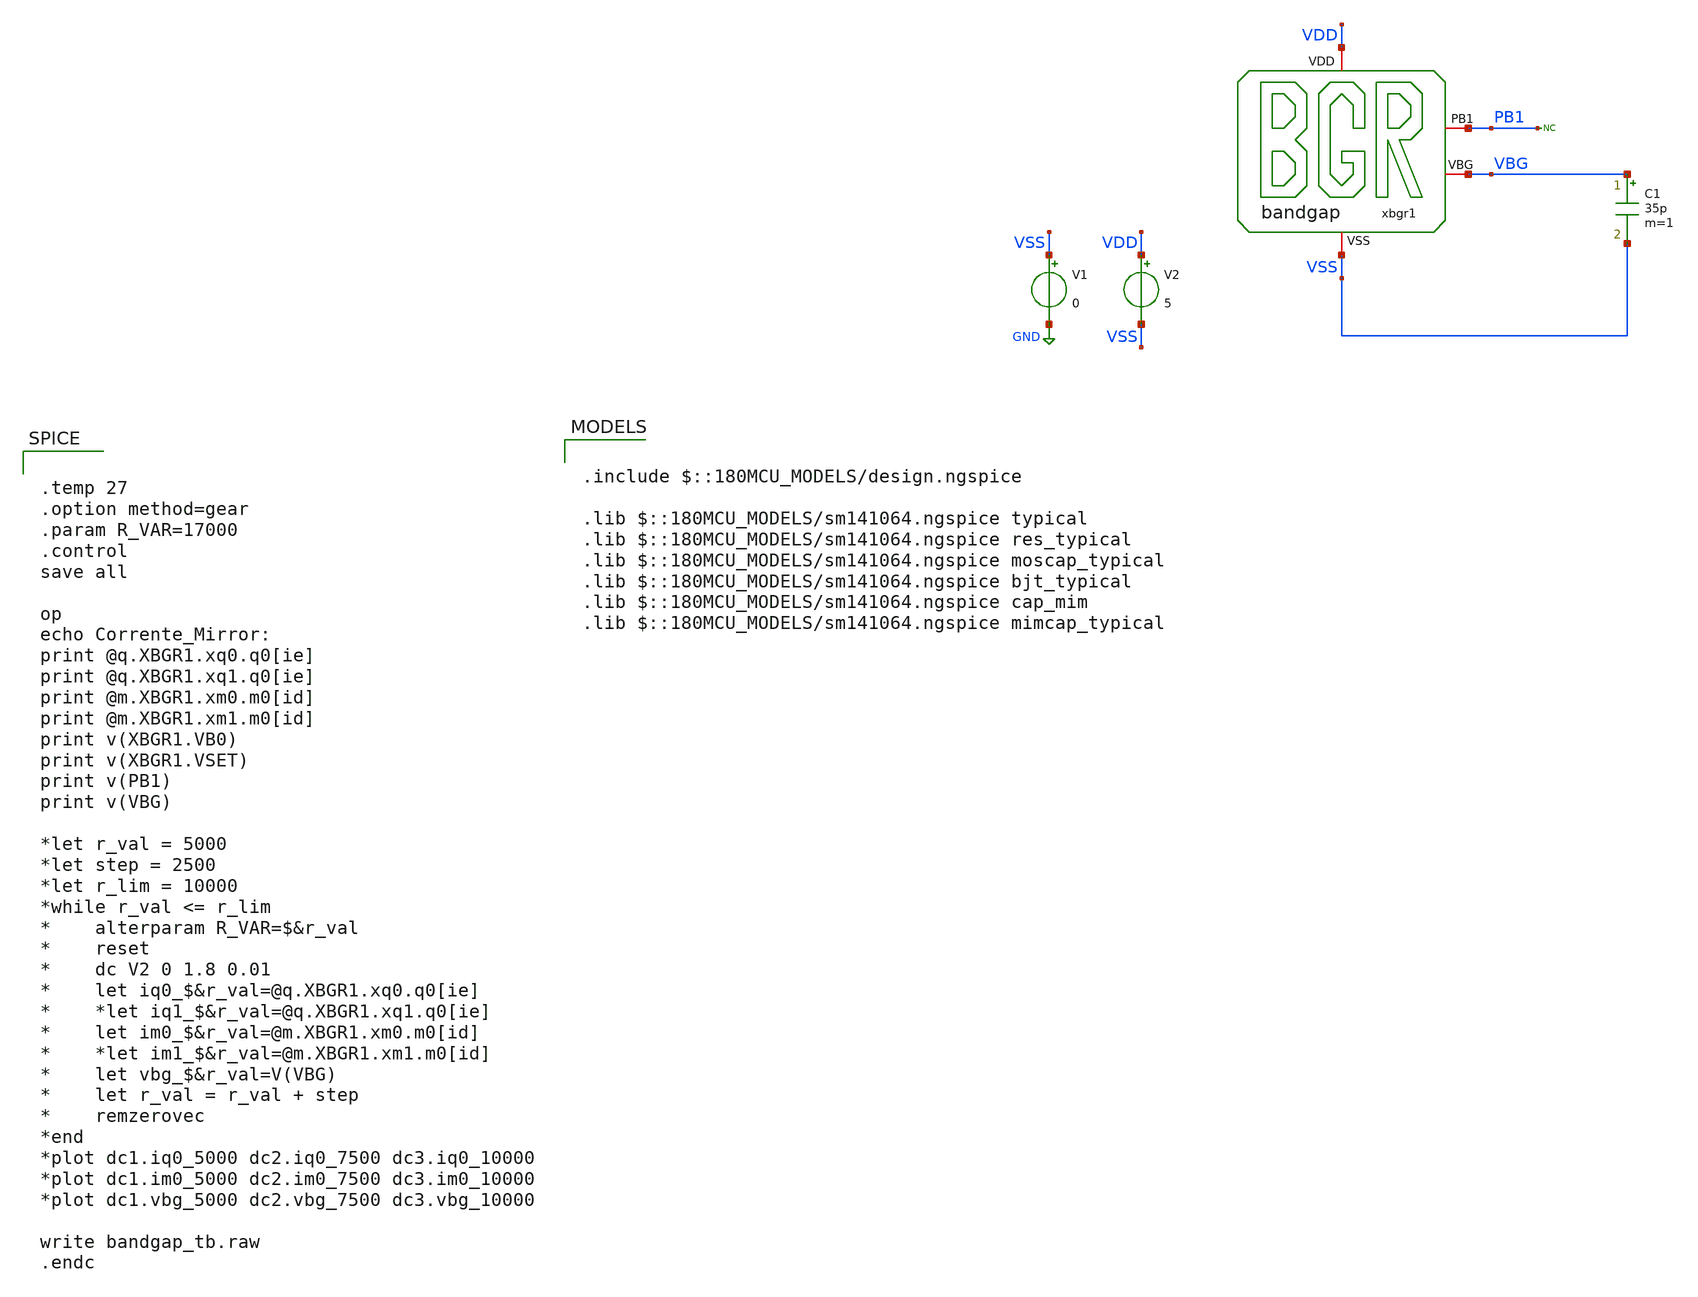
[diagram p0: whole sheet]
** sch_path: bandgap/xschem/sim/bandgap_tb_dc.sch
**.subckt bandgap_tb_dc
V1 VSS GND 0
V2 VDD VSS 5
C1 VBG VSS 35p m=1
* noconn PB1
xbgr1 VDD PB1 VBG VSS bandgap
**** begin user architecture code


.temp 27
.option method=gear
.param R_VAR=17000
.control
save all

op
echo Corrente_Mirror:
print @q.XBGR1.xq0.q0[ie]
print @q.XBGR1.xq1.q0[ie]
print @m.XBGR1.xm0.m0[id]
print @m.XBGR1.xm1.m0[id]
print v(XBGR1.VB0)
print v(XBGR1.VSET)
print v(PB1)
print v(VBG)

*let r_val = 5000
*let step = 2500
*let r_lim = 10000
*while r_val <= r_lim
*	alterparam R_VAR=$&r_val
*	reset
*	dc V2 0 1.8 0.01
*	let iq0_$&r_val=@q.XBGR1.xq0.q0[ie]
*	*let iq1_$&r_val=@q.XBGR1.xq1.q0[ie]
*	let im0_$&r_val=@m.XBGR1.xm0.m0[id]
*	*let im1_$&r_val=@m.XBGR1.xm1.m0[id]
*	let vbg_$&r_val=V(VBG)
*	let r_val = r_val + step
*	remzerovec
*end
*plot dc1.iq0_5000 dc2.iq0_7500 dc3.iq0_10000
*plot dc1.im0_5000 dc2.im0_7500 dc3.im0_10000
*plot dc1.vbg_5000 dc2.vbg_7500 dc3.vbg_10000

write bandgap_tb.raw
.endc



.include $::180MCU_MODELS/design.ngspice

.lib $::180MCU_MODELS/sm141064.ngspice typical
.lib $::180MCU_MODELS/sm141064.ngspice res_typical
.lib $::180MCU_MODELS/sm141064.ngspice moscap_typical
.lib $::180MCU_MODELS/sm141064.ngspice bjt_typical
.lib $::180MCU_MODELS/sm141064.ngspice cap_mim
.lib $::180MCU_MODELS/sm141064.ngspice mimcap_typical

**** end user architecture code
**.ends

* expanding   symbol:  bandgap/xschem/dev/bandgap.sym # of pins=4
** sym_path: bandgap/cace/testbenches/bandgap.sym
** sch_path: bandgap/cace/testbenches/bandgap.sch
.subckt bandgap VDD PB1 VBG VSS
*.iopin VSS
*.iopin VDD
*.iopin PB1
*.iopin VBG
R0 net7 VSET 1.7k m=1
R1 VSET VSS 7.6k m=1
R2 VB0 VBG 17000 m=1
XQ1 PB1 net8 net6 VSS npn_10p00x10p00 m=12
XQ0 VB0 VB0 net3 VSS npn_10p00x10p00 m=1
XM4 VSS net2 VSS VSS nfet_03v3 L=1u W=19u nf=1 ad='int((nf+1)/2) * W/nf * 0.18u' as='int((nf+2)/2) * W/nf * 0.18u'
+ pd='2*int((nf+1)/2) * (W/nf + 0.18u)' ps='2*int((nf+2)/2) * (W/nf + 0.18u)' nrd='0.18u / W' nrs='0.18u / W'
+ sa=0 sb=0 sd=0 m=1
XM2 net2 VSS VDD VDD pfet_03v3 L=10u W=1u nf=1 ad='int((nf+1)/2) * W/nf * 0.18u' as='int((nf+2)/2) * W/nf * 0.18u'
+ pd='2*int((nf+1)/2) * (W/nf + 0.18u)' ps='2*int((nf+2)/2) * (W/nf + 0.18u)' nrd='0.18u / W' nrs='0.18u / W'
+ sa=0 sb=0 sd=0 m=1
XM3 net5 net2 VDD VDD pfet_03v3 L=2u W=2u nf=1 ad='int((nf+1)/2) * W/nf * 0.18u' as='int((nf+2)/2) * W/nf * 0.18u'
+ pd='2*int((nf+1)/2) * (W/nf + 0.18u)' ps='2*int((nf+2)/2) * (W/nf + 0.18u)' nrd='0.18u / W' nrs='0.18u / W'
+ sa=0 sb=0 sd=0 m=1
XM1 net1 net1 VDD VDD pfet_03v3 L=7.4u W=20u nf=1 ad='int((nf+1)/2) * W/nf * 0.18u' as='int((nf+2)/2) * W/nf * 0.18u'
+ pd='2*int((nf+1)/2) * (W/nf + 0.18u)' ps='2*int((nf+2)/2) * (W/nf + 0.18u)' nrd='0.18u / W' nrs='0.18u / W'
+ sa=0 sb=0 sd=0 m=1
XM0 net4 net1 VDD VDD pfet_03v3 L=7.4u W=20u nf=1 ad='int((nf+1)/2) * W/nf * 0.18u' as='int((nf+2)/2) * W/nf * 0.18u'
+ pd='2*int((nf+1)/2) * (W/nf + 0.18u)' ps='2*int((nf+2)/2) * (W/nf + 0.18u)' nrd='0.18u / W' nrs='0.18u / W'
+ sa=0 sb=0 sd=0 m=1
VQ0E net3 VSET 0
VM0D net4 VB0 0
VM3D net5 VB0 0
VQ1E net6 net7 0
VM1D net1 PB1 0
VQ1B VBG net8 0
.ends

.GLOBAL GND
.end
